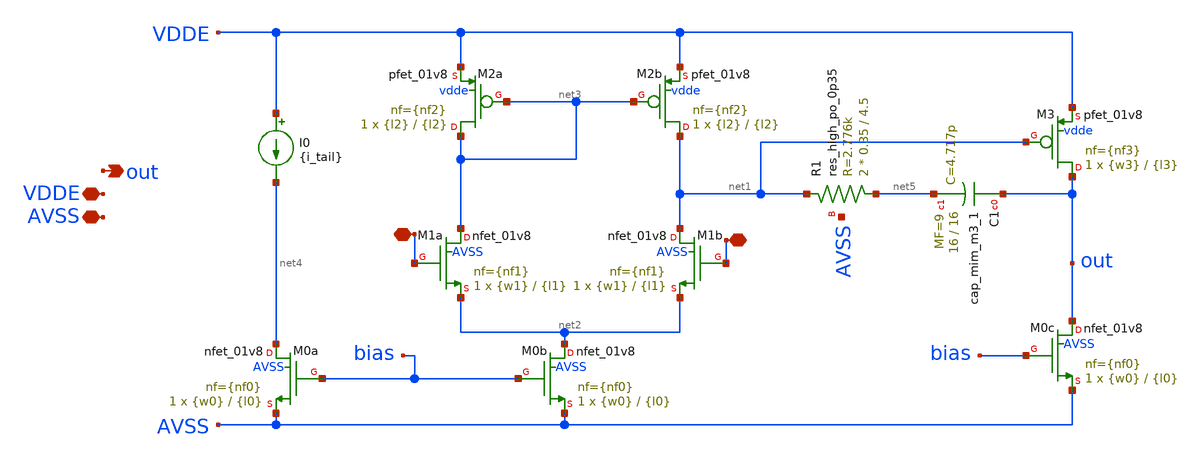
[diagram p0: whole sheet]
** sch_path: xschem/op.sch
**.subckt op AVSS - + VDDE out
*.iopin AVSS
*.iopin -
*.iopin +
*.iopin VDDE
*.opin out
XM2b net1 net3 VDDE vdde sky130_fd_pr__pfet_01v8 L={l2} W={l2} nf={nf2} ad='int((nf+1)/2) * W/nf * 0.29'
+ as='int((nf+2)/2) * W/nf * 0.29' pd='2*int((nf+1)/2) * (W/nf + 0.29)' ps='2*int((nf+2)/2) * (W/nf + 0.29)'
+ nrd='0.29 / W' nrs='0.29 / W' sa=0 sb=0 sd=0 mult=1 m=1
XM2a net3 net3 VDDE vdde sky130_fd_pr__pfet_01v8 L={l2} W={l2} nf={nf2} ad='int((nf+1)/2) * W/nf * 0.29'
+ as='int((nf+2)/2) * W/nf * 0.29' pd='2*int((nf+1)/2) * (W/nf + 0.29)' ps='2*int((nf+2)/2) * (W/nf + 0.29)'
+ nrd='0.29 / W' nrs='0.29 / W' sa=0 sb=0 sd=0 mult=1 m=1
XM3 out net1 VDDE vdde sky130_fd_pr__pfet_01v8 L={l3} W={w3} nf={nf3} ad='int((nf+1)/2) * W/nf * 0.29'
+ as='int((nf+2)/2) * W/nf * 0.29' pd='2*int((nf+1)/2) * (W/nf + 0.29)' ps='2*int((nf+2)/2) * (W/nf + 0.29)'
+ nrd='0.29 / W' nrs='0.29 / W' sa=0 sb=0 sd=0 mult=1 m=1
XM0c out bias AVSS AVSS sky130_fd_pr__nfet_01v8 L={l0} W={w0} nf={nf0} ad='int((nf+1)/2) * W/nf * 0.29'
+ as='int((nf+2)/2) * W/nf * 0.29' pd='2*int((nf+1)/2) * (W/nf + 0.29)' ps='2*int((nf+2)/2) * (W/nf + 0.29)'
+ nrd='0.29 / W' nrs='0.29 / W' sa=0 sb=0 sd=0 mult=1 m=1
XM1b net1 + net2 AVSS sky130_fd_pr__nfet_01v8 L={l1} W={w1} nf={nf1} ad='int((nf+1)/2) * W/nf * 0.29'
+ as='int((nf+2)/2) * W/nf * 0.29' pd='2*int((nf+1)/2) * (W/nf + 0.29)' ps='2*int((nf+2)/2) * (W/nf + 0.29)'
+ nrd='0.29 / W' nrs='0.29 / W' sa=0 sb=0 sd=0 mult=1 m=1
XM1a net3 - net2 AVSS sky130_fd_pr__nfet_01v8 L={l1} W={w1} nf={nf1} ad='int((nf+1)/2) * W/nf * 0.29'
+ as='int((nf+2)/2) * W/nf * 0.29' pd='2*int((nf+1)/2) * (W/nf + 0.29)' ps='2*int((nf+2)/2) * (W/nf + 0.29)'
+ nrd='0.29 / W' nrs='0.29 / W' sa=0 sb=0 sd=0 mult=1 m=1
XR1 net5 net1 AVSS sky130_fd_pr__res_high_po_0p35 L=4.5 mult=2 m=2
XC1 out net5 sky130_fd_pr__cap_mim_m3_1 W=16 L=16 MF=9 m=9
I0 VDDE net4 {i_tail}
XM0b net2 bias AVSS AVSS sky130_fd_pr__nfet_01v8 L={l0} W={w0} nf={nf0} ad='int((nf+1)/2) * W/nf * 0.29'
+ as='int((nf+2)/2) * W/nf * 0.29' pd='2*int((nf+1)/2) * (W/nf + 0.29)' ps='2*int((nf+2)/2) * (W/nf + 0.29)'
+ nrd='0.29 / W' nrs='0.29 / W' sa=0 sb=0 sd=0 mult=1 m=1
XM0a net4 bias AVSS AVSS sky130_fd_pr__nfet_01v8 L={l0} W={w0} nf={nf0} ad='int((nf+1)/2) * W/nf * 0.29'
+ as='int((nf+2)/2) * W/nf * 0.29' pd='2*int((nf+1)/2) * (W/nf + 0.29)' ps='2*int((nf+2)/2) * (W/nf + 0.29)'
+ nrd='0.29 / W' nrs='0.29 / W' sa=0 sb=0 sd=0 mult=1 m=1
**.ends
.end
